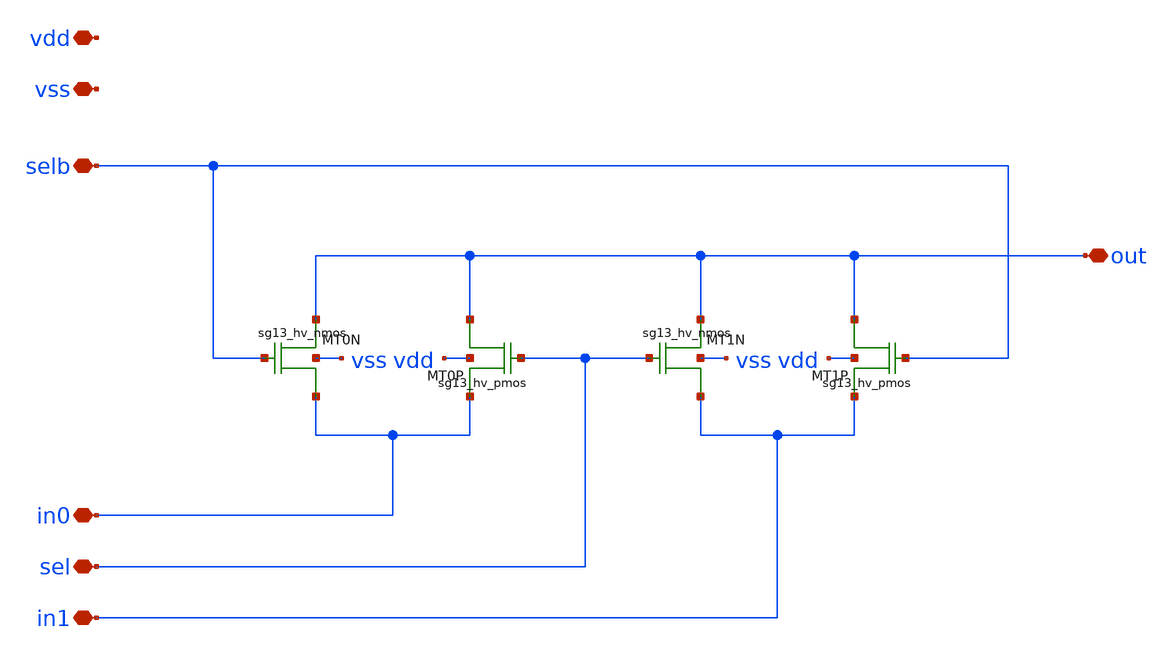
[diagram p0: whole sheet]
** sch_path: xschem/logic_gates/MUXHV.sch
**.subckt MUXHV out in0 in1 sel selb vdd vss
*.iopin out
*.iopin in0
*.iopin in1
*.iopin sel
*.iopin selb
*.iopin vdd
*.iopin vss
XMT0N out selb in0 vss sg13_hv_nmos w=1.5u l=0.45u ng=1 m=1
XMT0P in0 sel out vdd sg13_hv_pmos w=3.0u l=0.45u ng=1 m=1
XMT1N out sel in1 vss sg13_hv_nmos w=1.5u l=0.45u ng=1 m=1
XMT1P in1 selb out vdd sg13_hv_pmos w=3.0u l=0.45u ng=1 m=1
**.ends
.end
